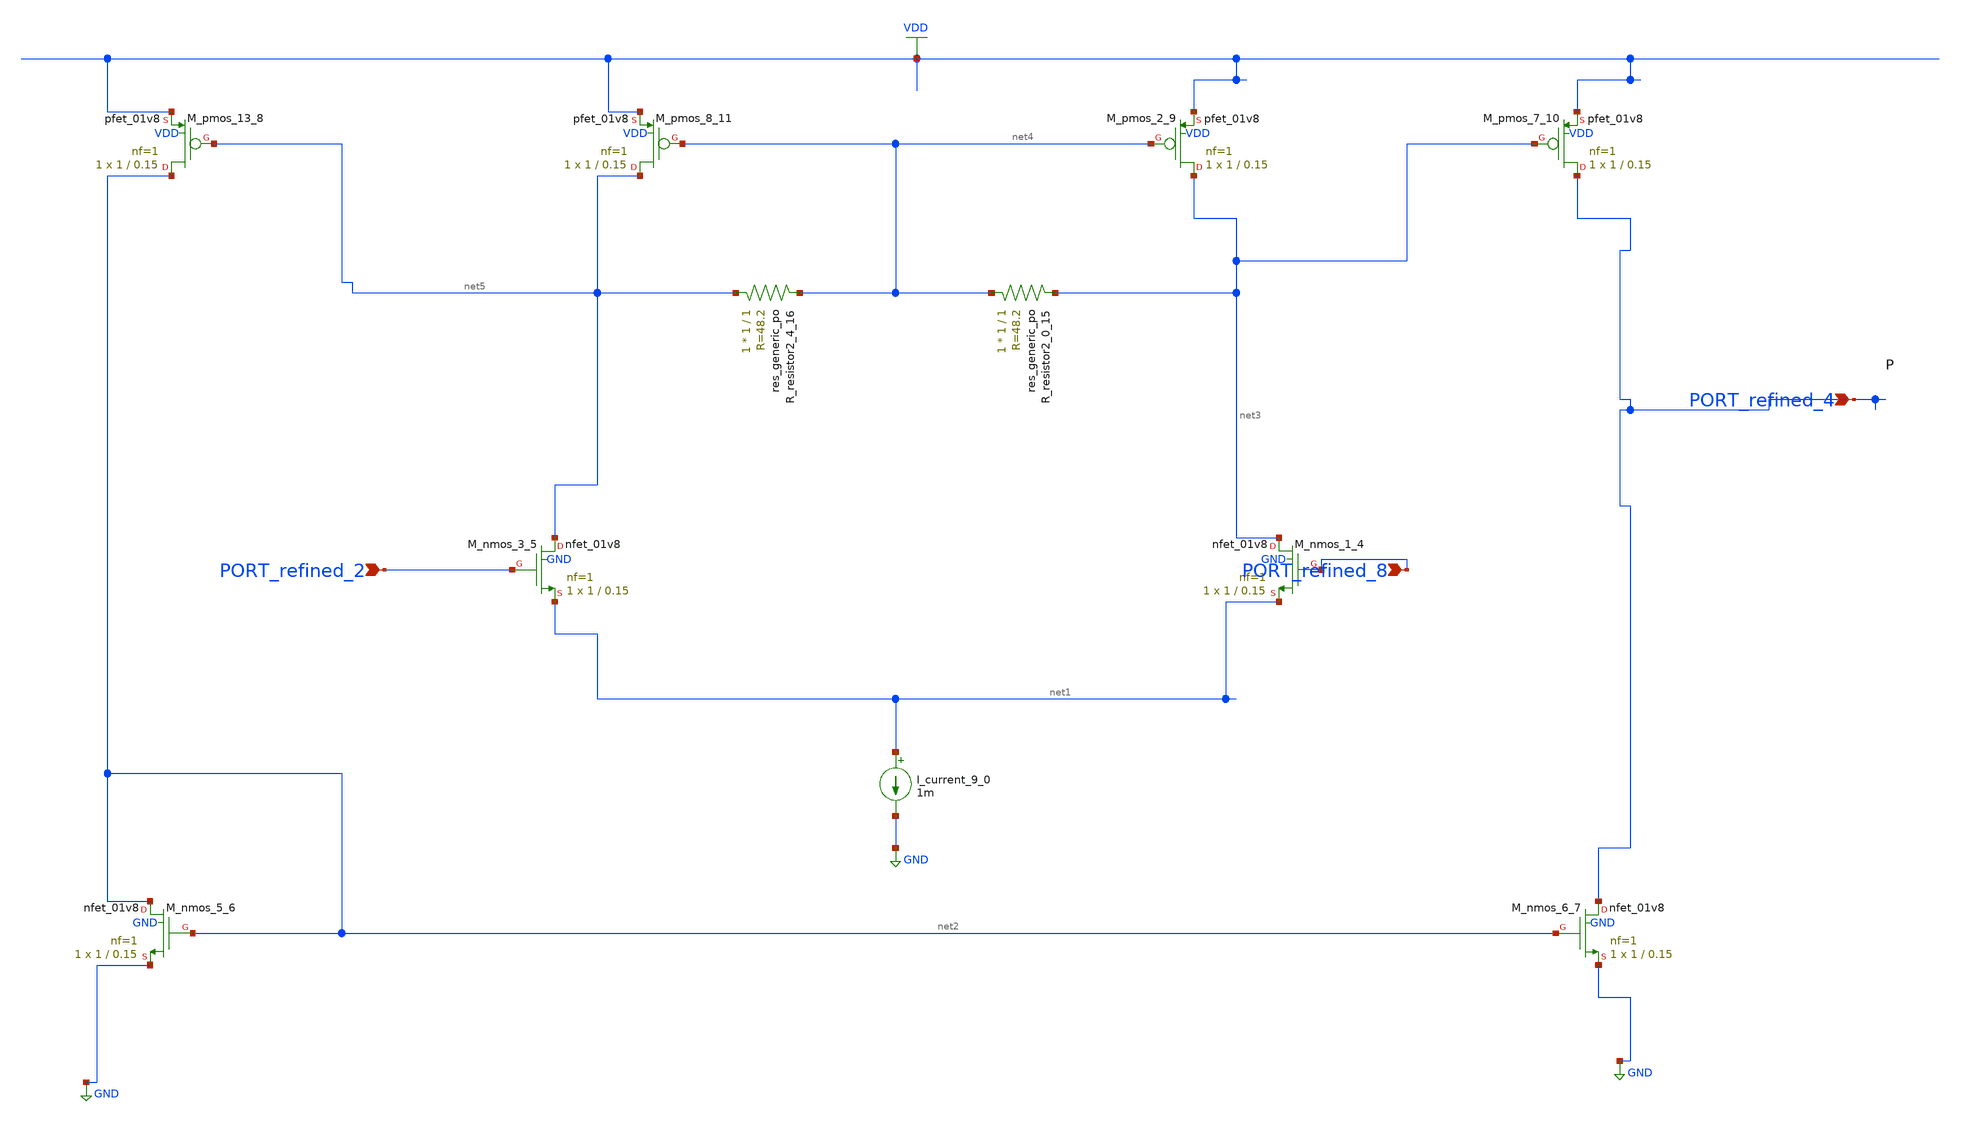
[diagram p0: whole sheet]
** sch_path: schematics/SchemGen/10_1051_itmconf_20235402010_07_001.sch
**.subckt 10_1051_itmconf_20235402010_07_001 PORT_refined_2 PORT_refined_8 PORT_refined_4
*.ipin PORT_refined_2
*.ipin PORT_refined_8
*.ipin PORT_refined_4
I_current_9_0 net1 GND 1m
XM_nmos_1_4 net3 PORT_refined_8 net1 GND sky130_fd_pr__nfet_01v8 L=0.15 W=1 nf=1 ad='int((1 + 1)/2) * 1 / 1 * 0.29'
+ as='int((1 + 2)/2) * 1 / 1 * 0.29' pd='2*int((1 + 1)/2) * (1 / 1 + 0.29)' ps='2*int((1 + 2)/2) * (1 / 1 + 0.29)'
+ nrd='0.29 / 1 ' nrs='0.29 / 1 ' sa=0 sb=0 sd=0 mult=1 m=1
XM_nmos_3_5 net5 PORT_refined_2 net1 GND sky130_fd_pr__nfet_01v8 L=0.15 W=1 nf=1 ad='int((1 + 1)/2) * 1 / 1 * 0.29'
+ as='int((1 + 2)/2) * 1 / 1 * 0.29' pd='2*int((1 + 1)/2) * (1 / 1 + 0.29)' ps='2*int((1 + 2)/2) * (1 / 1 + 0.29)'
+ nrd='0.29 / 1 ' nrs='0.29 / 1 ' sa=0 sb=0 sd=0 mult=1 m=1
XM_nmos_5_6 net2 net2 GND GND sky130_fd_pr__nfet_01v8 L=0.15 W=1 nf=1 ad='int((1 + 1)/2) * 1 / 1 * 0.29'
+ as='int((1 + 2)/2) * 1 / 1 * 0.29' pd='2*int((1 + 1)/2) * (1 / 1 + 0.29)' ps='2*int((1 + 2)/2) * (1 / 1 + 0.29)'
+ nrd='0.29 / 1 ' nrs='0.29 / 1 ' sa=0 sb=0 sd=0 mult=1 m=1
XM_nmos_6_7 PORT_refined_4 net2 GND GND sky130_fd_pr__nfet_01v8 L=0.15 W=1 nf=1 ad='int((1 + 1)/2) * 1 / 1 * 0.29'
+ as='int((1 + 2)/2) * 1 / 1 * 0.29' pd='2*int((1 + 1)/2) * (1 / 1 + 0.29)' ps='2*int((1 + 2)/2) * (1 / 1 + 0.29)'
+ nrd='0.29 / 1 ' nrs='0.29 / 1 ' sa=0 sb=0 sd=0 mult=1 m=1
XM_pmos_13_8 net2 net5 VDD VDD sky130_fd_pr__pfet_01v8 L=0.15 W=1 nf=1 ad='int((1 + 1)/2) * 1 / 1 * 0.29'
+ as='int((1 + 2)/2) * 1 / 1 * 0.29' pd='2*int((1 + 1)/2) * (1 / 1 + 0.29)' ps='2*int((1 + 2)/2) * (1 / 1 + 0.29)'
+ nrd='0.29 / 1 ' nrs='0.29 / 1 ' sa=0 sb=0 sd=0 mult=1 m=1
XM_pmos_2_9 net3 net4 VDD VDD sky130_fd_pr__pfet_01v8 L=0.15 W=1 nf=1 ad='int((1 + 1)/2) * 1 / 1 * 0.29'
+ as='int((1 + 2)/2) * 1 / 1 * 0.29' pd='2*int((1 + 1)/2) * (1 / 1 + 0.29)' ps='2*int((1 + 2)/2) * (1 / 1 + 0.29)'
+ nrd='0.29 / 1 ' nrs='0.29 / 1 ' sa=0 sb=0 sd=0 mult=1 m=1
XM_pmos_7_10 PORT_refined_4 net3 VDD VDD sky130_fd_pr__pfet_01v8 L=0.15 W=1 nf=1 ad='int((1 + 1)/2) * 1 / 1 * 0.29'
+ as='int((1 + 2)/2) * 1 / 1 * 0.29' pd='2*int((1 + 1)/2) * (1 / 1 + 0.29)' ps='2*int((1 + 2)/2) * (1 / 1 + 0.29)'
+ nrd='0.29 / 1 ' nrs='0.29 / 1 ' sa=0 sb=0 sd=0 mult=1 m=1
XM_pmos_8_11 net5 net4 VDD VDD sky130_fd_pr__pfet_01v8 L=0.15 W=1 nf=1 ad='int((1 + 1)/2) * 1 / 1 * 0.29'
+ as='int((1 + 2)/2) * 1 / 1 * 0.29' pd='2*int((1 + 1)/2) * (1 / 1 + 0.29)' ps='2*int((1 + 2)/2) * (1 / 1 + 0.29)'
+ nrd='0.29 / 1 ' nrs='0.29 / 1 ' sa=0 sb=0 sd=0 mult=1 m=1
XR_resistor2_0_15 net4 net3 sky130_fd_pr__res_generic_po W=1 L=1 m=1
XR_resistor2_4_16 net5 net4 sky130_fd_pr__res_generic_po W=1 L=1 m=1
**.ends
.GLOBAL GND
.GLOBAL VDD
.end
